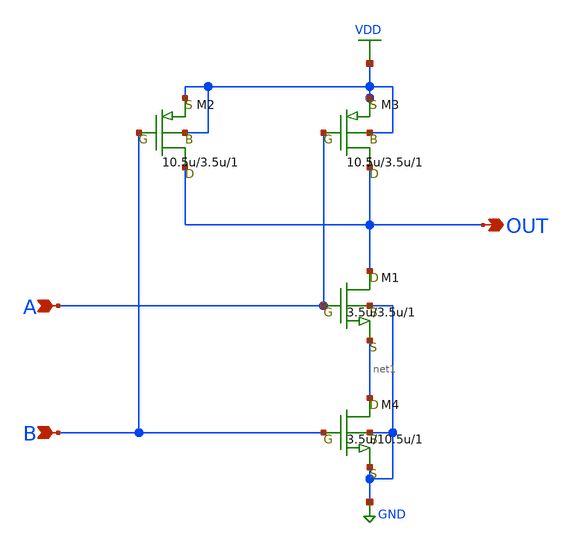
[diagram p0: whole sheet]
** sch_path: LR_hokari/LR_Work2/symbol/2NANDLR.sch
**.subckt 2NANDLR A B OUT
*.ipin A
*.ipin B
*.opin OUT
M1 OUT A net1 GND nch w=3.5u l=3.5u as=0 ps=0 ad=0 pd=0 m=1
M2 OUT B VDD VDD pch w=10.5u l=3.5u as=0 ps=0 ad=0 pd=0 m=1
M3 OUT A VDD VDD pch w=10.5u l=3.5u as=0 ps=0 ad=0 pd=0 m=1
M4 net1 B GND GND nch w=3.5u l=10.5u as=0 ps=0 ad=0 pd=0 m=1
**.ends
.GLOBAL VDD
.GLOBAL GND
.end
